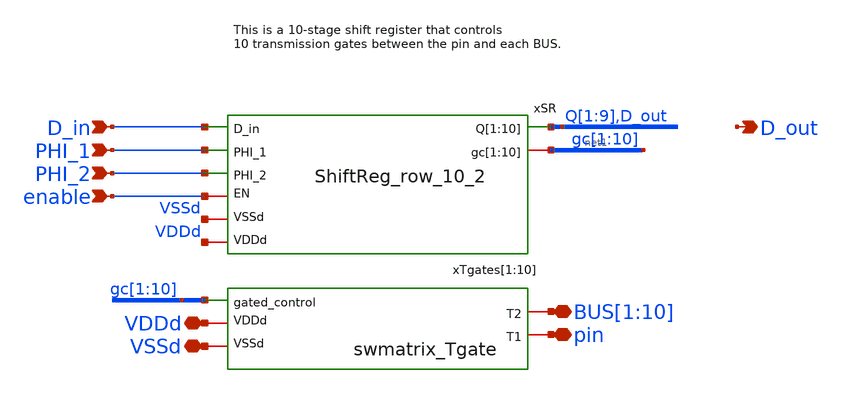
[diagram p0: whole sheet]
** sch_path: swmatrix_row_10/swmatrix_row_10.sch
**.subckt swmatrix_row_10 pin PHI_2 PHI_1
*+ BUS[1],BUS[2],BUS[3],BUS[4],BUS[5],BUS[6],BUS[7],BUS[8],BUS[9],BUS[10] D_in D_out VDDd VSSd enable
*.iopin pin
*.ipin PHI_2
*.ipin PHI_1
*.iopin BUS[1],BUS[2],BUS[3],BUS[4],BUS[5],BUS[6],BUS[7],BUS[8],BUS[9],BUS[10]
*.ipin D_in
*.opin D_out
*.iopin VDDd
*.iopin VSSd
*.ipin enable
xSR D_in Q[1] Q[2] Q[3] Q[4] Q[5] Q[6] Q[7] Q[8] Q[9] D_out net1[9] net1[8] net1[7] net1[6] net1[5]
+ net1[4] net1[3] net1[2] net1[1] net1[0] PHI_1 PHI_2 net2 VDDd VSSd ShiftReg_row_10_2
xTgates[1] gc[1] BUS[1] pin VSSd VDDd swmatrix_Tgate
xTgates[2] gc[2] BUS[2] pin VSSd VDDd swmatrix_Tgate
xTgates[3] gc[3] BUS[3] pin VSSd VDDd swmatrix_Tgate
xTgates[4] gc[4] BUS[4] pin VSSd VDDd swmatrix_Tgate
xTgates[5] gc[5] BUS[5] pin VSSd VDDd swmatrix_Tgate
xTgates[6] gc[6] BUS[6] pin VSSd VDDd swmatrix_Tgate
xTgates[7] gc[7] BUS[7] pin VSSd VDDd swmatrix_Tgate
xTgates[8] gc[8] BUS[8] pin VSSd VDDd swmatrix_Tgate
xTgates[9] gc[9] BUS[9] pin VSSd VDDd swmatrix_Tgate
xTgates[10] gc[10] BUS[10] pin VSSd VDDd swmatrix_Tgate
**.ends
.end
